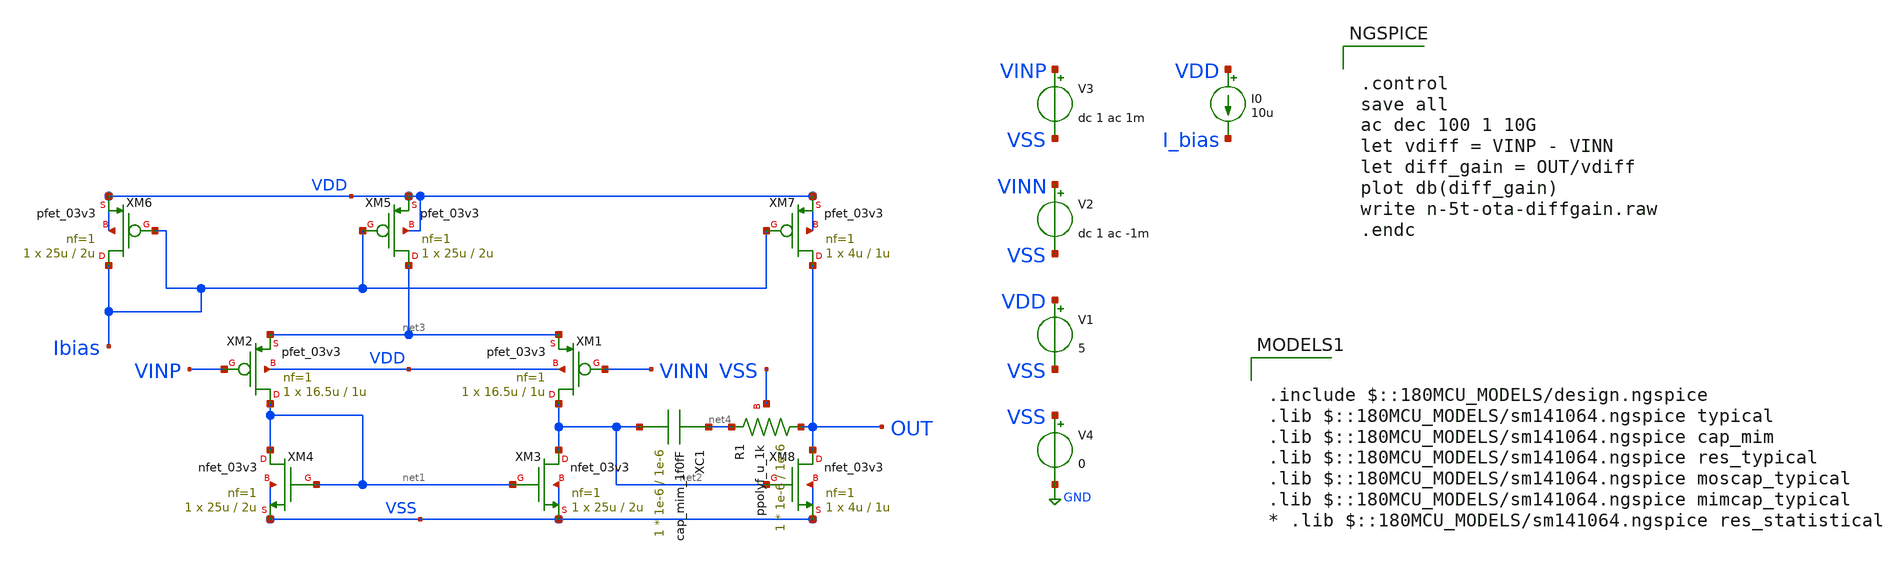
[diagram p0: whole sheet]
** sch_path: week02_current_diffpair/tugas5_cascode_current_mirror/2stage-pmos-ota.sch
**.subckt 2stage-pmos-ota
XM1 net2 VINN net3 VDD pfet_03v3 L=1u W=16.5u nf=1 ad='int((nf+1)/2) * W/nf * 0.18u' as='int((nf+2)/2) * W/nf * 0.18u'
+ pd='2*int((nf+1)/2) * (W/nf + 0.18u)' ps='2*int((nf+2)/2) * (W/nf + 0.18u)' nrd='0.18u / W' nrs='0.18u / W'
+ sa=0 sb=0 sd=0 m=1
XM2 net1 VINP net3 VDD pfet_03v3 L=1u W=16.5u nf=1 ad='int((nf+1)/2) * W/nf * 0.18u' as='int((nf+2)/2) * W/nf * 0.18u'
+ pd='2*int((nf+1)/2) * (W/nf + 0.18u)' ps='2*int((nf+2)/2) * (W/nf + 0.18u)' nrd='0.18u / W' nrs='0.18u / W'
+ sa=0 sb=0 sd=0 m=1
XM3 net2 net1 VSS VSS nfet_03v3 L=2u W=25u nf=1 ad='int((nf+1)/2) * W/nf * 0.18u' as='int((nf+2)/2) * W/nf * 0.18u'
+ pd='2*int((nf+1)/2) * (W/nf + 0.18u)' ps='2*int((nf+2)/2) * (W/nf + 0.18u)' nrd='0.18u / W' nrs='0.18u / W'
+ sa=0 sb=0 sd=0 m=1
XM4 net1 net1 VSS VSS nfet_03v3 L=2u W=25u nf=1 ad='int((nf+1)/2) * W/nf * 0.18u' as='int((nf+2)/2) * W/nf * 0.18u'
+ pd='2*int((nf+1)/2) * (W/nf + 0.18u)' ps='2*int((nf+2)/2) * (W/nf + 0.18u)' nrd='0.18u / W' nrs='0.18u / W'
+ sa=0 sb=0 sd=0 m=1
XM5 net3 Ibias VDD VDD pfet_03v3 L=2u W=25u nf=1 ad='int((nf+1)/2) * W/nf * 0.18u' as='int((nf+2)/2) * W/nf * 0.18u'
+ pd='2*int((nf+1)/2) * (W/nf + 0.18u)' ps='2*int((nf+2)/2) * (W/nf + 0.18u)' nrd='0.18u / W' nrs='0.18u / W'
+ sa=0 sb=0 sd=0 m=1
XM6 Ibias Ibias VDD VDD pfet_03v3 L=2u W=25u nf=1 ad='int((nf+1)/2) * W/nf * 0.18u' as='int((nf+2)/2) * W/nf * 0.18u'
+ pd='2*int((nf+1)/2) * (W/nf + 0.18u)' ps='2*int((nf+2)/2) * (W/nf + 0.18u)' nrd='0.18u / W' nrs='0.18u / W'
+ sa=0 sb=0 sd=0 m=1
XM7 OUT Ibias VDD VDD pfet_03v3 L=1u W=4u nf=1 ad='int((nf+1)/2) * W/nf * 0.18u' as='int((nf+2)/2) * W/nf * 0.18u'
+ pd='2*int((nf+1)/2) * (W/nf + 0.18u)' ps='2*int((nf+2)/2) * (W/nf + 0.18u)' nrd='0.18u / W' nrs='0.18u / W'
+ sa=0 sb=0 sd=0 m=1
XM8 OUT net2 VSS VSS nfet_03v3 L=1u W=4u nf=1 ad='int((nf+1)/2) * W/nf * 0.18u' as='int((nf+2)/2) * W/nf * 0.18u'
+ pd='2*int((nf+1)/2) * (W/nf + 0.18u)' ps='2*int((nf+2)/2) * (W/nf + 0.18u)' nrd='0.18u / W' nrs='0.18u / W'
+ sa=0 sb=0 sd=0 m=1
V1 VDD VSS 5
V2 VINN VSS dc 1 ac -1m
V3 VINP VSS dc 1 ac 1m
V4 VSS GND 0
I0 VDD I_bias 10u
XC1 net4 net2 cap_mim_1f0fF c_width=1e-6 c_length=1e-6 m=1
XR1 OUT net4 VSS ppolyf_u_1k r_width=1e-6 r_length=1e-6 m=1
**** begin user architecture code


.control
save all
ac dec 100 1 10G
let vdiff = VINP - VINN
let diff_gain = OUT/vdiff
plot db(diff_gain)
write n-5t-ota-diffgain.raw
.endc



.include $::180MCU_MODELS/design.ngspice
.lib $::180MCU_MODELS/sm141064.ngspice typical
.lib $::180MCU_MODELS/sm141064.ngspice cap_mim
.lib $::180MCU_MODELS/sm141064.ngspice res_typical
.lib $::180MCU_MODELS/sm141064.ngspice moscap_typical
.lib $::180MCU_MODELS/sm141064.ngspice mimcap_typical
* .lib $::180MCU_MODELS/sm141064.ngspice res_statistical

**** end user architecture code
**.ends
.GLOBAL GND
.end
